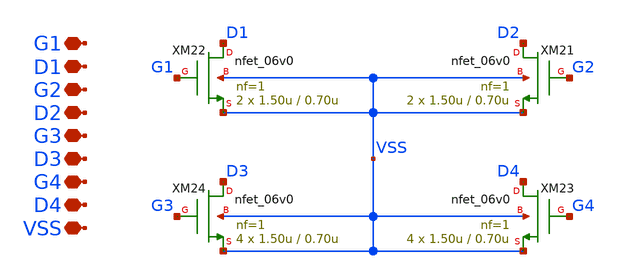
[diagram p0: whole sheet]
** sch_path: designs/libs/core_single-fet/nfet-com/nfet-com.sch
**.subckt nfet-com VSS D1 G1 D2 G2 D3 G3 D4 G4
*.iopin VSS
*.iopin D1
*.iopin G1
*.iopin D2
*.iopin G2
*.iopin D3
*.iopin G3
*.iopin D4
*.iopin G4
XM21 D2 G2 VSS VSS nfet_06v0 L=0.70u W=1.50u nf=1 ad='int((nf+1)/2) * W/nf * 0.18u' as='int((nf+2)/2) * W/nf * 0.18u'
+ pd='2*int((nf+1)/2) * (W/nf + 0.18u)' ps='2*int((nf+2)/2) * (W/nf + 0.18u)' nrd='0.18u / W' nrs='0.18u / W'
+ sa=0 sb=0 sd=0 m=2
XM22 D1 G1 VSS VSS nfet_06v0 L=0.70u W=1.50u nf=1 ad='int((nf+1)/2) * W/nf * 0.18u' as='int((nf+2)/2) * W/nf * 0.18u'
+ pd='2*int((nf+1)/2) * (W/nf + 0.18u)' ps='2*int((nf+2)/2) * (W/nf + 0.18u)' nrd='0.18u / W' nrs='0.18u / W'
+ sa=0 sb=0 sd=0 m=2
XM23 D4 G4 VSS VSS nfet_06v0 L=0.70u W=1.50u nf=1 ad='int((nf+1)/2) * W/nf * 0.18u' as='int((nf+2)/2) * W/nf * 0.18u'
+ pd='2*int((nf+1)/2) * (W/nf + 0.18u)' ps='2*int((nf+2)/2) * (W/nf + 0.18u)' nrd='0.18u / W' nrs='0.18u / W'
+ sa=0 sb=0 sd=0 m=4
XM24 D3 G3 VSS VSS nfet_06v0 L=0.70u W=1.50u nf=1 ad='int((nf+1)/2) * W/nf * 0.18u' as='int((nf+2)/2) * W/nf * 0.18u'
+ pd='2*int((nf+1)/2) * (W/nf + 0.18u)' ps='2*int((nf+2)/2) * (W/nf + 0.18u)' nrd='0.18u / W' nrs='0.18u / W'
+ sa=0 sb=0 sd=0 m=4
**.ends
.end
